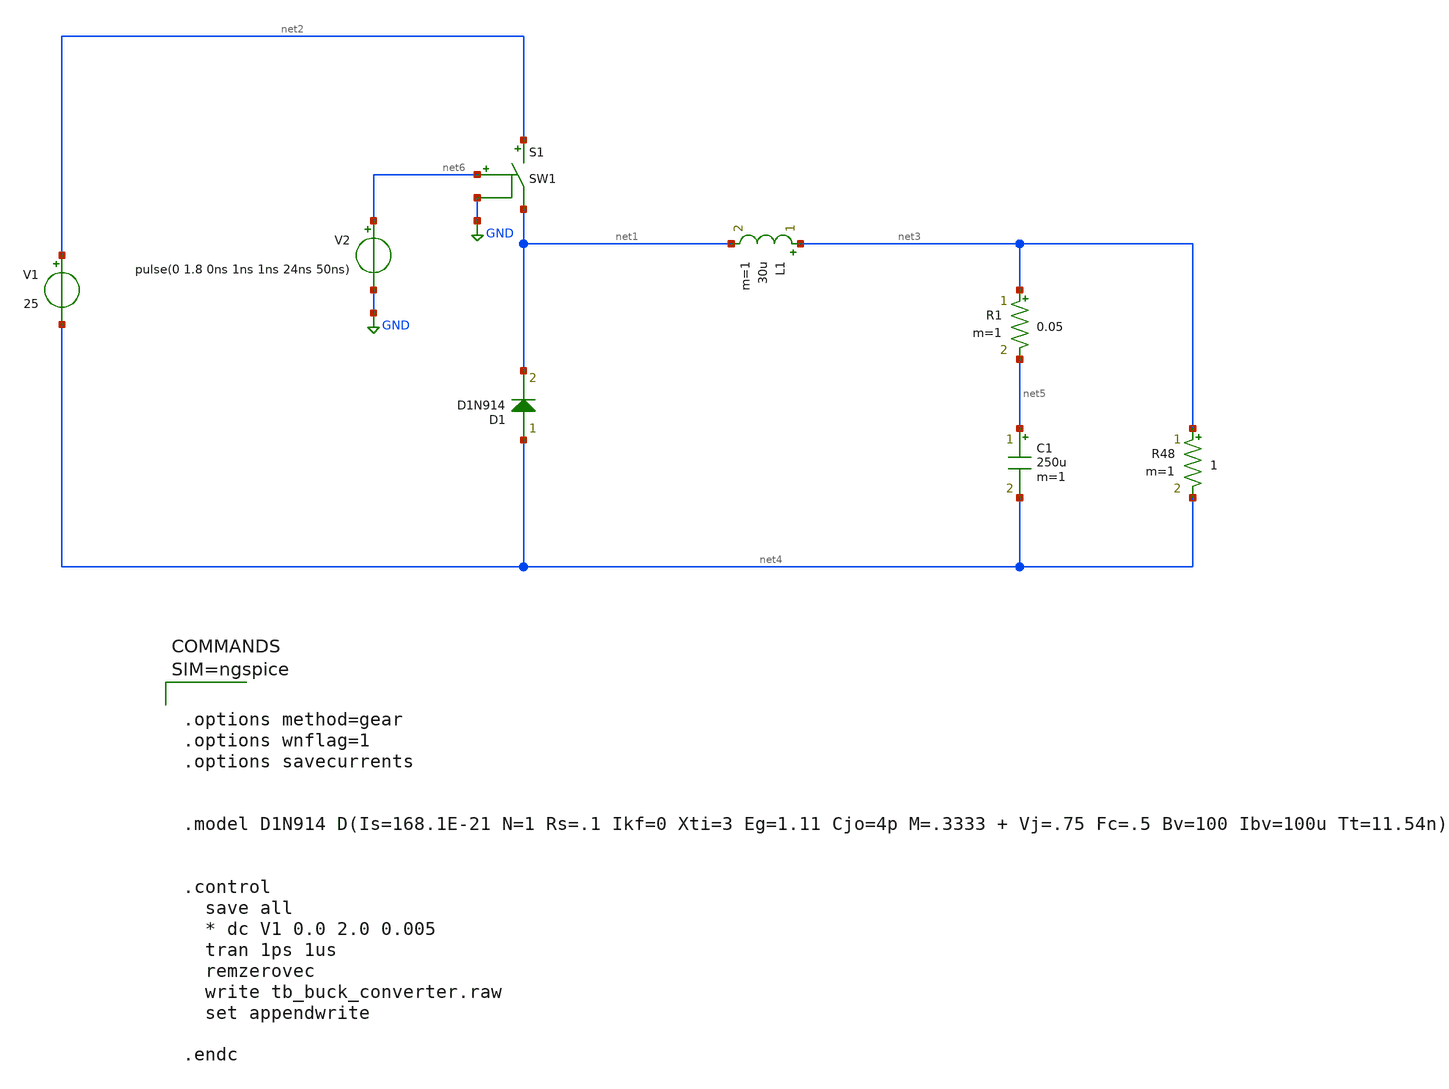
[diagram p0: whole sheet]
** sch_path: projects/ASU/EEE572/schematic/tb_buck_converter.sch
**.subckt tb_buck_converter
V1 net2 net4 25
R48 net3 net4 1 m=1
D1 net4 net1 D1N914 area=1
L1 net3 net1 30u m=1
C1 net5 net4 250u m=1
R1 net3 net5 0.05 m=1
V2 net6 GND pulse(0 1.8 0ns 1ns 1ns 24ns 50ns)
S1 net2 net1 net6 GND SW1
**** begin user architecture code



.options method=gear
.options wnflag=1
.options savecurrents


.model D1N914 D(Is=168.1E-21 N=1 Rs=.1 Ikf=0 Xti=3 Eg=1.11 Cjo=4p M=.3333 + Vj=.75 Fc=.5 Bv=100
+ Ibv=100u Tt=11.54n)


.control
  save all
  * dc V1 0.0 2.0 0.005
  tran 1ps 1us
  remzerovec
  write tb_buck_converter.raw
  set appendwrite

.endc





**** end user architecture code
**.ends
.GLOBAL GND
**** begin user architecture code
.MODEL SW1 SW( VT=0.9 VH=0.01 RON=0.01 ROFF=10G )
**** end user architecture code
.end
